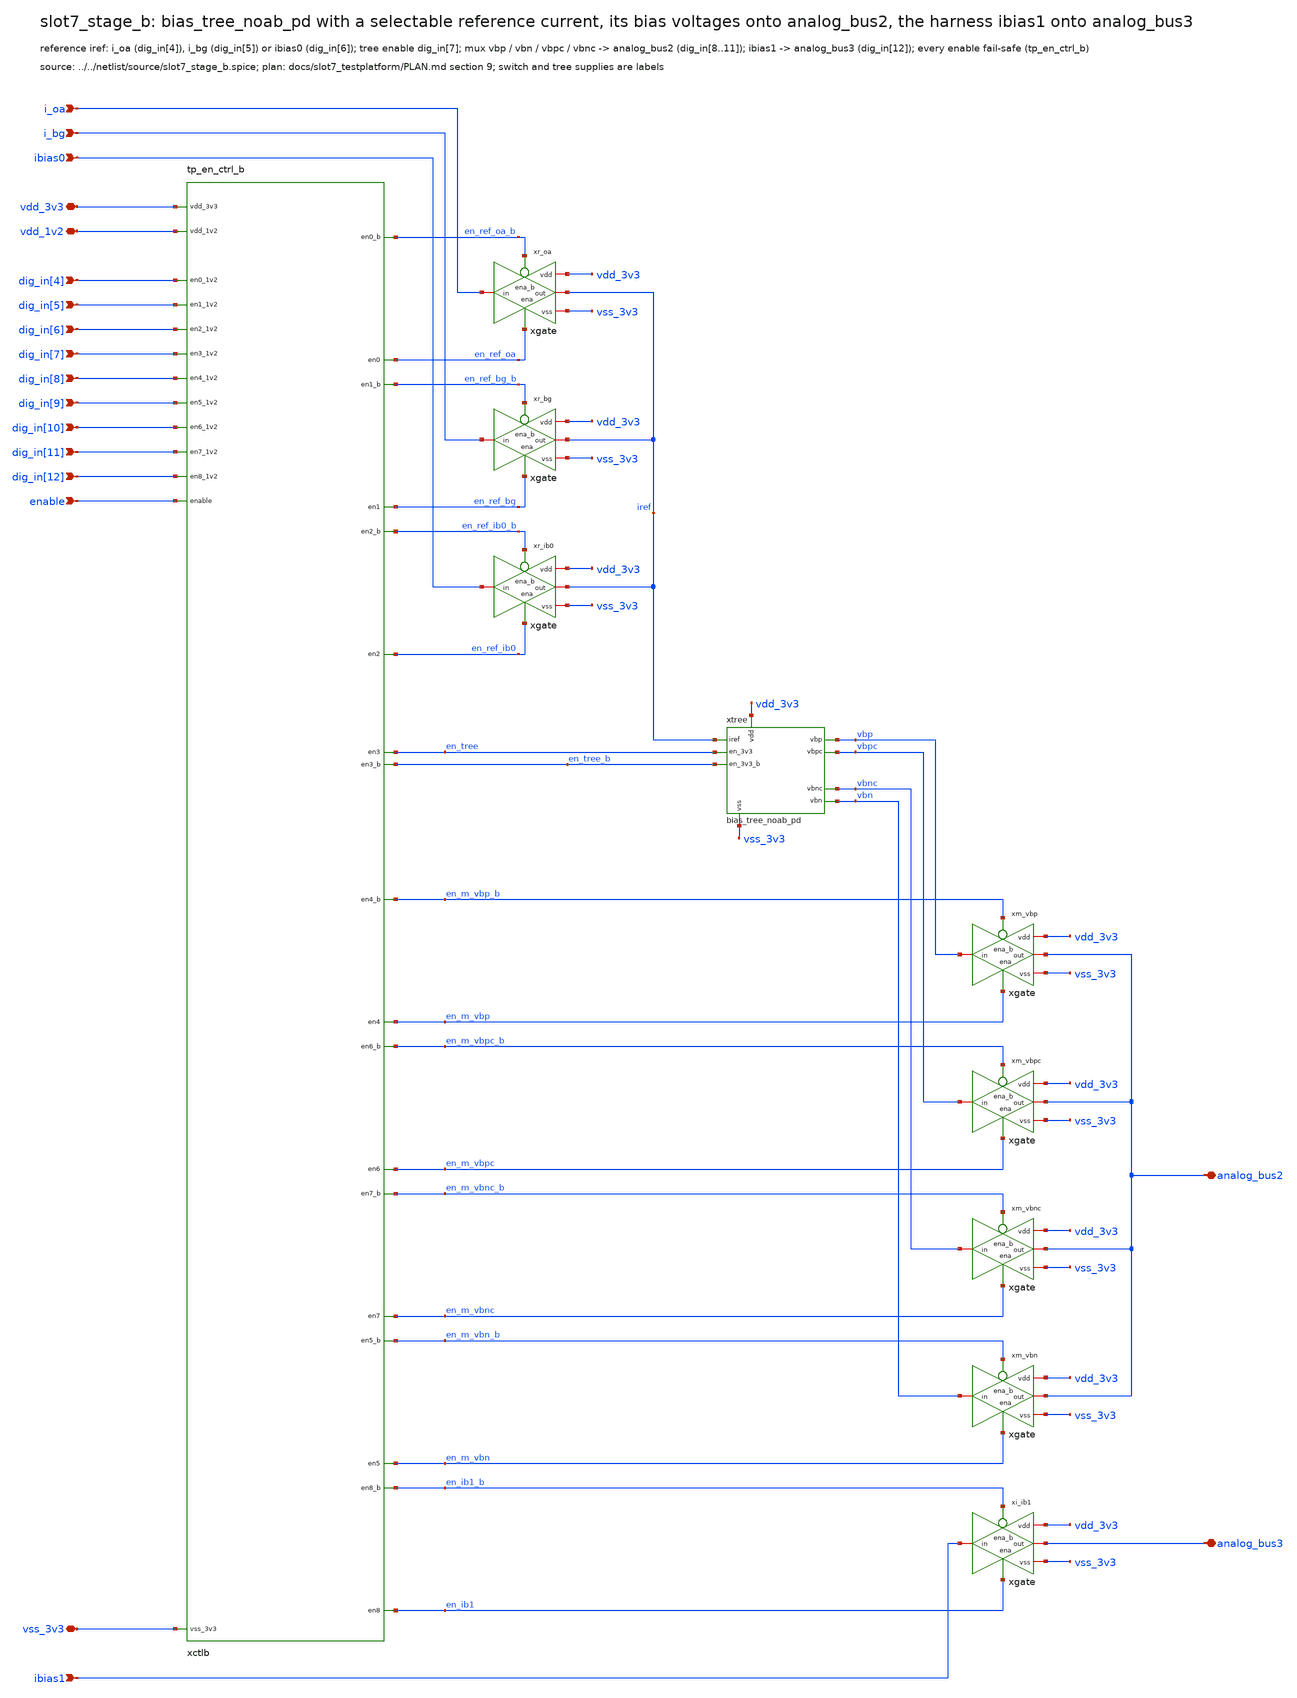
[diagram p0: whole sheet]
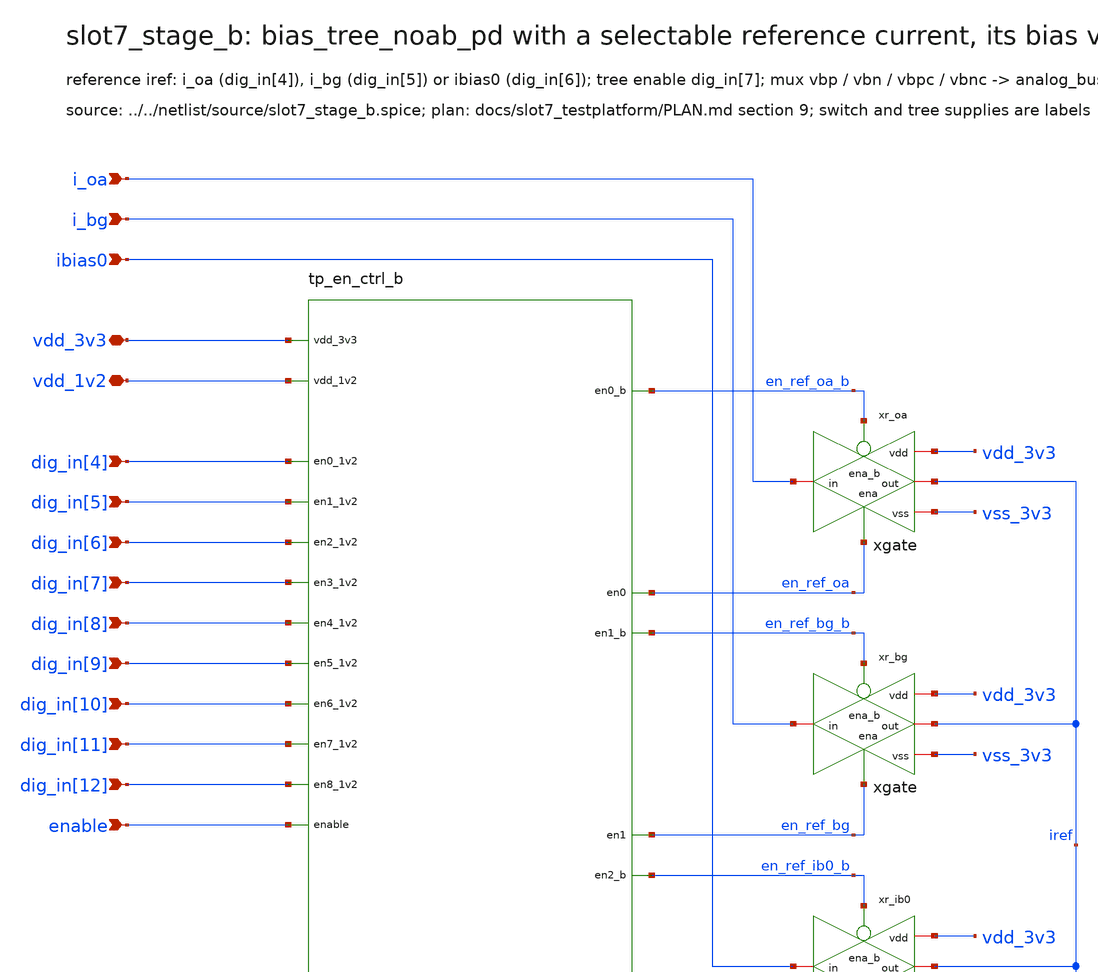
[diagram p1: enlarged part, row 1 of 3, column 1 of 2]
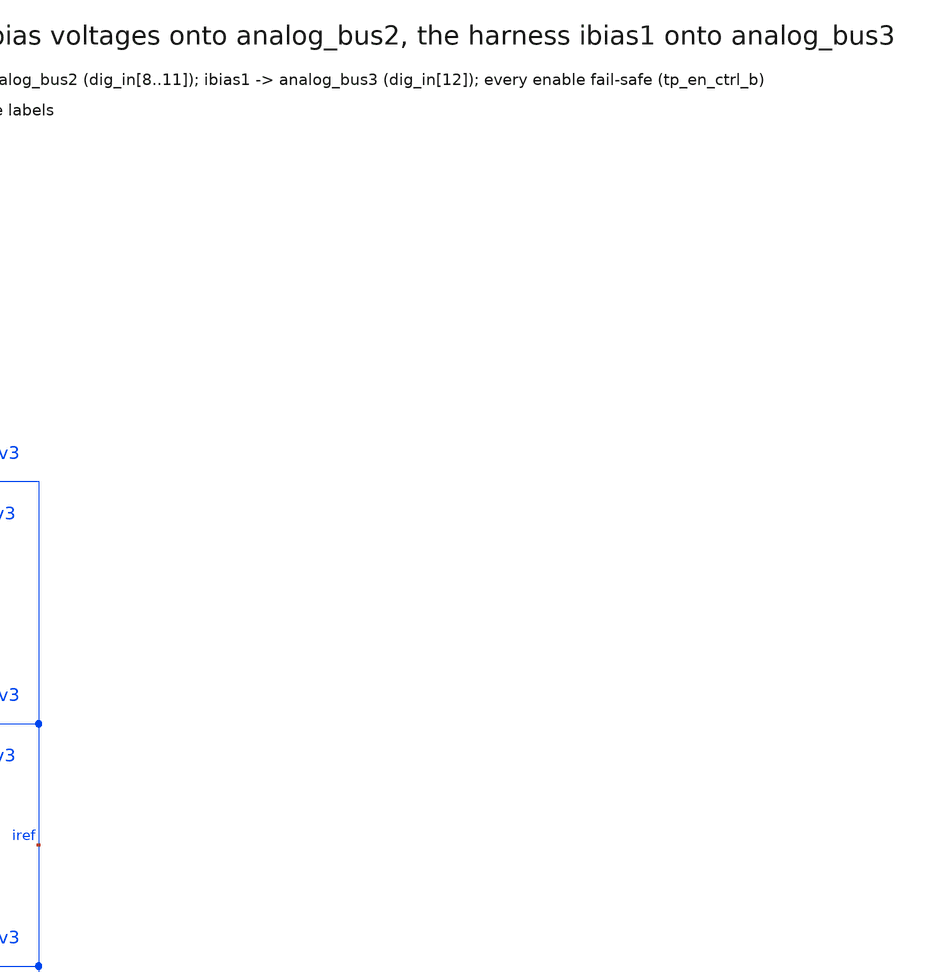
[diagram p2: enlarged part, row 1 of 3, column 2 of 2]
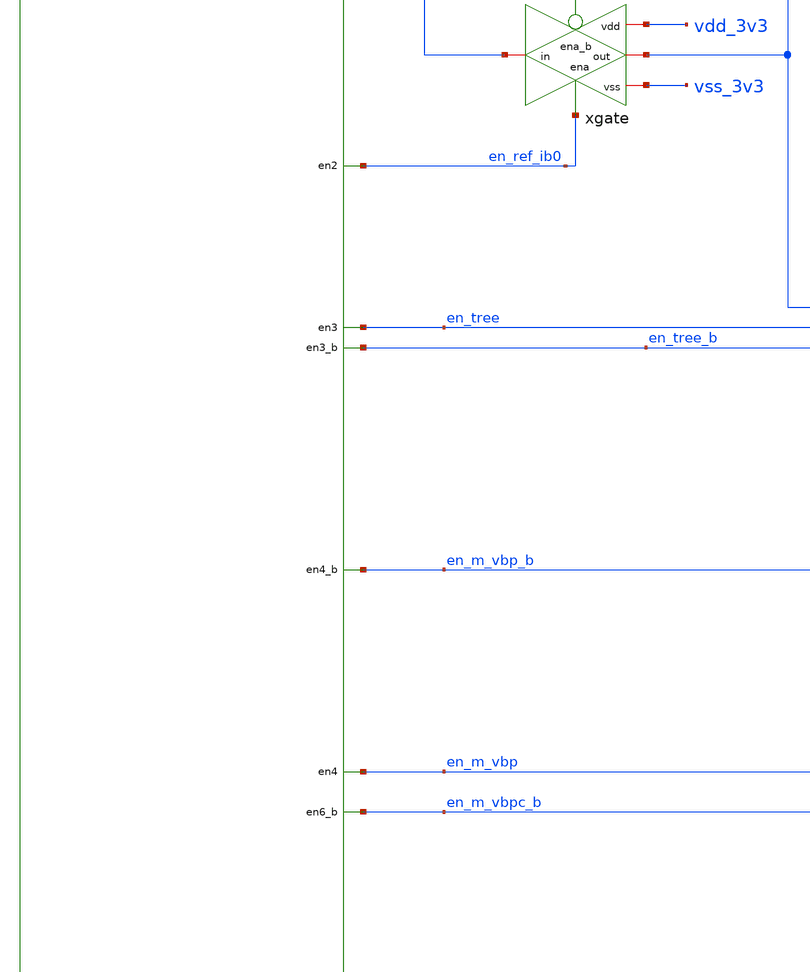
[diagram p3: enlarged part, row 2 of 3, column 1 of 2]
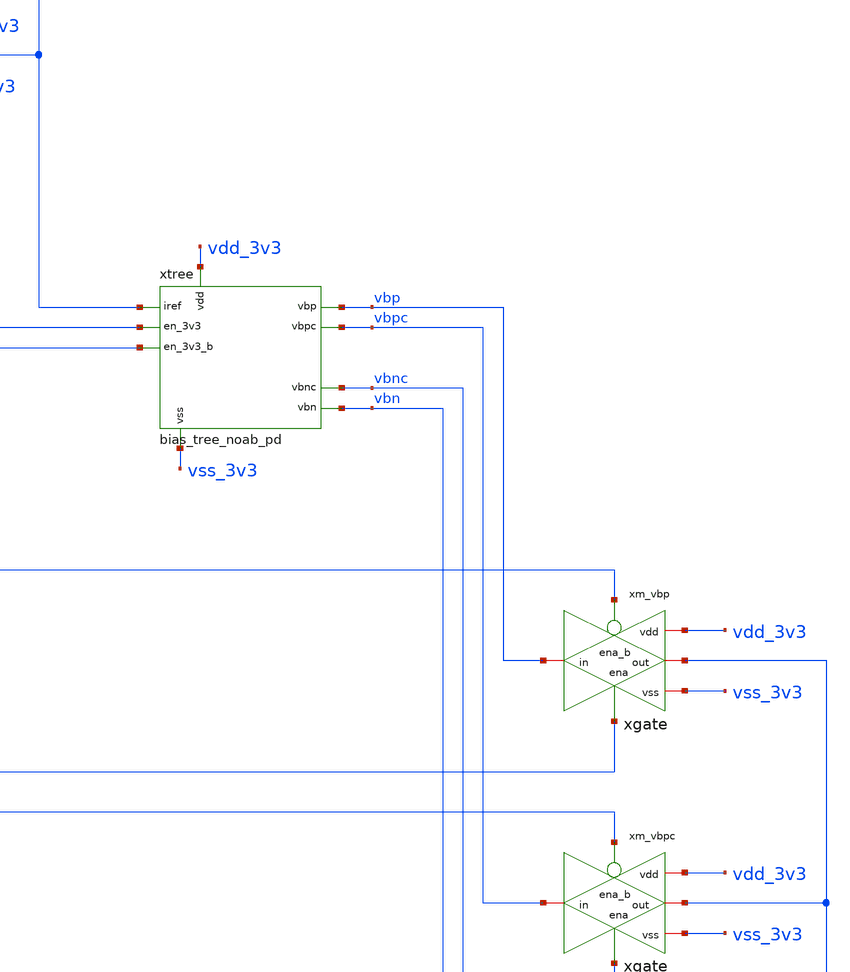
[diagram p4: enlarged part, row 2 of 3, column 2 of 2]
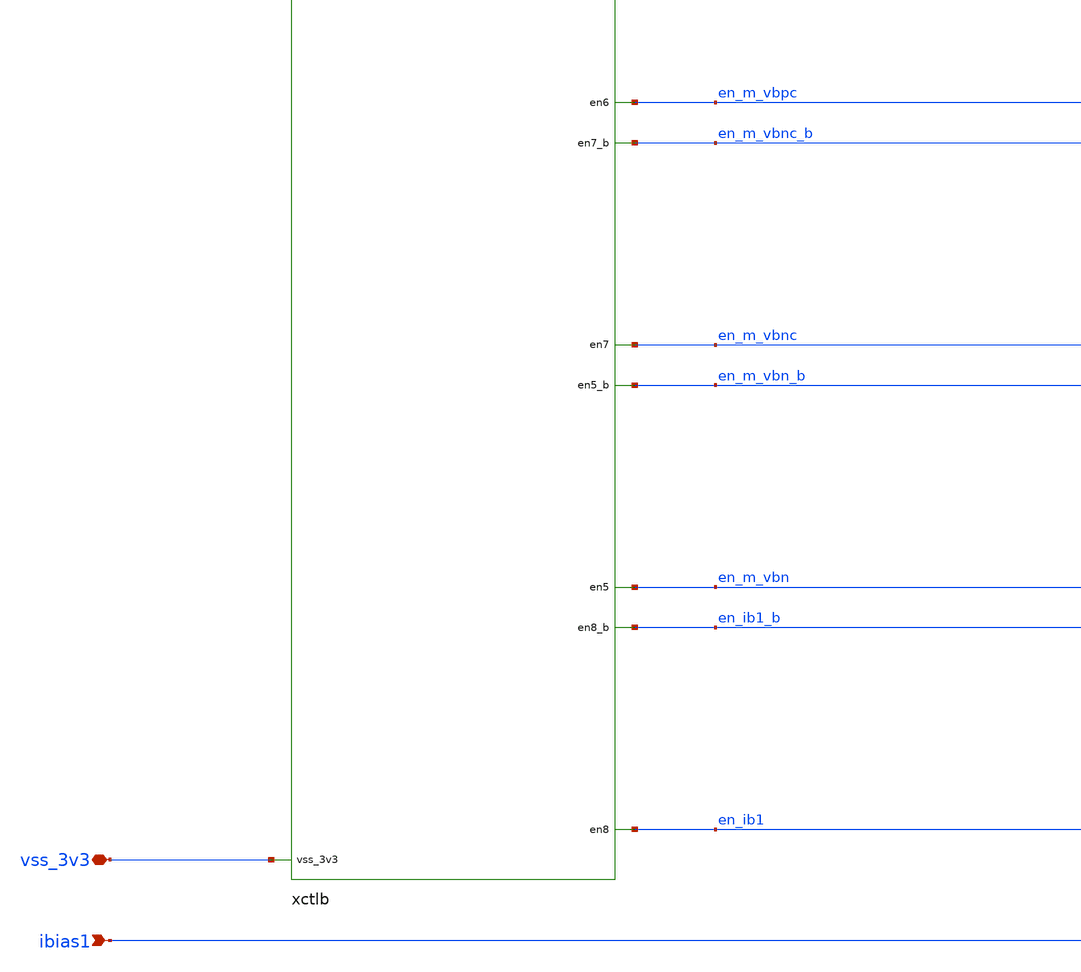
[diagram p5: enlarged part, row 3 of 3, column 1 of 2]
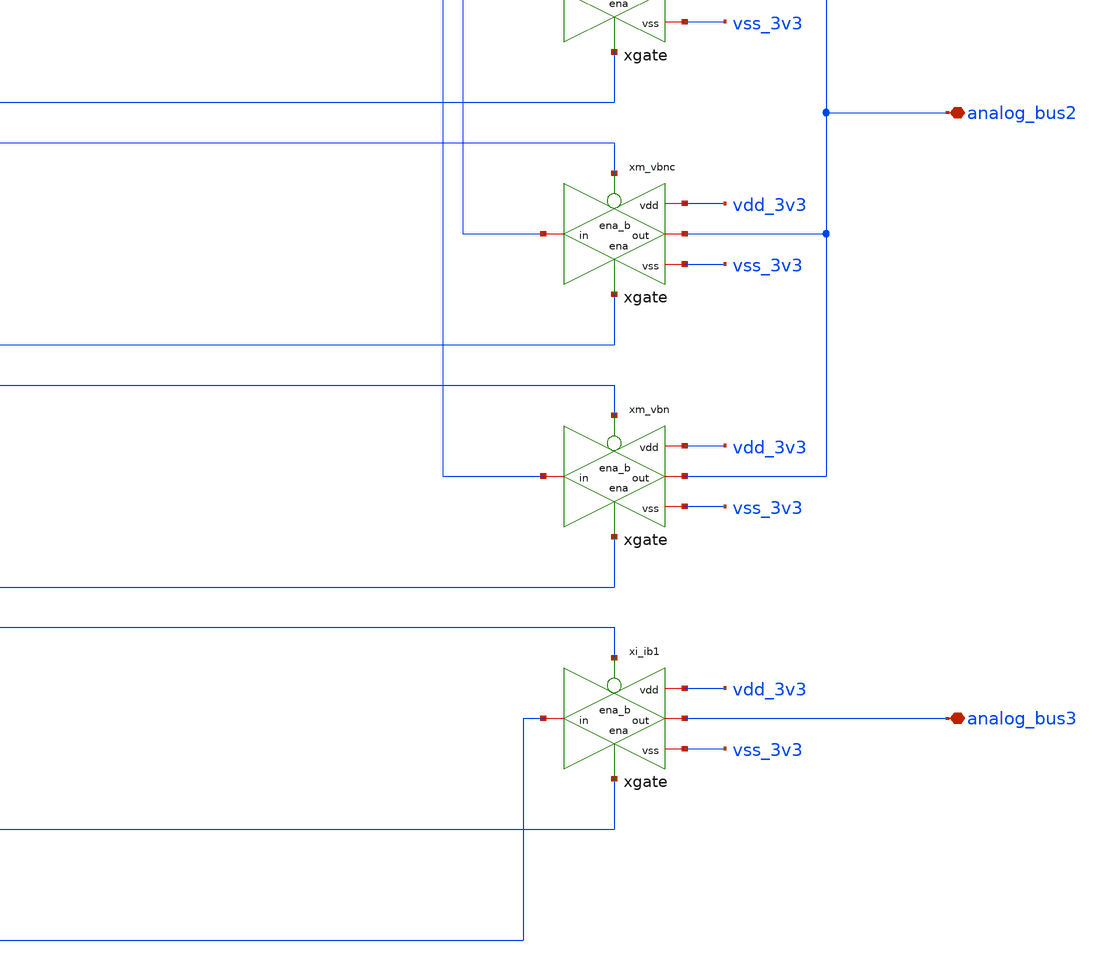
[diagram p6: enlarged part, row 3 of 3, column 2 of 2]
** sch_path: macros/slot7_testplatform/schematic/xschem_drawn/slot7_stage_b.sch
**.subckt slot7_stage_b vdd_3v3 vss_3v3 vdd_1v2 enable dig_in[4] dig_in[5] dig_in[6] dig_in[7]
*+ dig_in[8] dig_in[9] dig_in[10] dig_in[11] dig_in[12] i_oa i_bg ibias0 ibias1 analog_bus2 analog_bus3
*.iopin vdd_3v3
*.iopin vss_3v3
*.iopin vdd_1v2
*.ipin enable
*.ipin dig_in[4]
*.ipin dig_in[5]
*.ipin dig_in[6]
*.ipin dig_in[7]
*.ipin dig_in[8]
*.ipin dig_in[9]
*.ipin dig_in[10]
*.ipin dig_in[11]
*.ipin dig_in[12]
*.ipin i_oa
*.ipin i_bg
*.ipin ibias0
*.ipin ibias1
*.iopin analog_bus2
*.iopin analog_bus3
xctlb vdd_3v3 vss_3v3 vdd_1v2 dig_in[4] dig_in[5] dig_in[6] dig_in[7] dig_in[8] dig_in[9] dig_in[10]
+ dig_in[11] dig_in[12] enable en_ref_oa en_ref_oa_b en_ref_bg en_ref_bg_b en_ref_ib0 en_ref_ib0_b en_tree
+ en_tree_b en_m_vbp en_m_vbp_b en_m_vbn en_m_vbn_b en_m_vbpc en_m_vbpc_b en_m_vbnc en_m_vbnc_b en_ib1 en_ib1_b
+ tp_en_ctrl_b
xr_oa en_ref_oa_b vdd_3v3 i_oa iref vss_3v3 en_ref_oa xgate
xr_bg en_ref_bg_b vdd_3v3 i_bg iref vss_3v3 en_ref_bg xgate
xr_ib0 en_ref_ib0_b vdd_3v3 ibias0 iref vss_3v3 en_ref_ib0 xgate
xtree vdd_3v3 vss_3v3 iref vbp vbn vbpc vbnc en_tree en_tree_b bias_tree_noab_pd
xm_vbp en_m_vbp_b vdd_3v3 vbp analog_bus2 vss_3v3 en_m_vbp xgate
xm_vbpc en_m_vbpc_b vdd_3v3 vbpc analog_bus2 vss_3v3 en_m_vbpc xgate
xm_vbnc en_m_vbnc_b vdd_3v3 vbnc analog_bus2 vss_3v3 en_m_vbnc xgate
xm_vbn en_m_vbn_b vdd_3v3 vbn analog_bus2 vss_3v3 en_m_vbn xgate
xi_ib1 en_ib1_b vdd_3v3 ibias1 analog_bus3 vss_3v3 en_ib1 xgate
**.ends
.end
